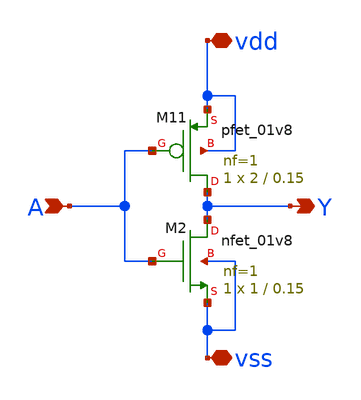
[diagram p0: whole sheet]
** sch_path: xschem/Logic/sky130A_inv1.sch
* Copyright 2021 Stefan Frederik Schippers
* Licensed under the Apache License, Version 2.0 (the "License");
* you may not use this file except in compliance with the License.
* You may obtain a copy of the License at
* https://www.apache.org/licenses/LICENSE-2.0
* Unless required by applicable law or agreed to in writing, software
* distributed under the License is distributed on an "AS IS" BASIS,
* WITHOUT WARRANTIES OR CONDITIONS OF ANY KIND, either express or implied.
* See the License for the specific language governing permissions and
* limitations under the License.
**.subckt sky130A_inv1 A Y vdd vss
*.ipin A
*.opin Y
*.iopin vdd
*.iopin vss
XM11 Y A vdd vdd sky130_fd_pr__pfet_01v8 L=0.15 W=2 nf=1 ad='int((nf+1)/2) * W/nf * 0.29' as='int((nf+2)/2) * W/nf * 0.29'
+ pd='2*int((nf+1)/2) * (W/nf + 0.29)' ps='2*int((nf+2)/2) * (W/nf + 0.29)' nrd='0.29 / W' nrs='0.29 / W'
+ sa=0 sb=0 sd=0 mult=1 m=1
XM2 Y A vss vss sky130_fd_pr__nfet_01v8 L=0.15 W=1 nf=1 ad='int((1 + 1)/2) * 1 / 1 * 0.29' as='int((1 + 2)/2) * 1 / 1 * 0.29'
+ pd='2*int((1 + 1)/2) * (1 / 1 + 0.29)' ps='2*int((1 + 2)/2) * (1 / 1 + 0.29)' nrd='0.29 / 1 ' nrs='0.29 / 1 '
+ sa=0 sb=0 sd=0 mult=1 m=1
**.ends
.end
